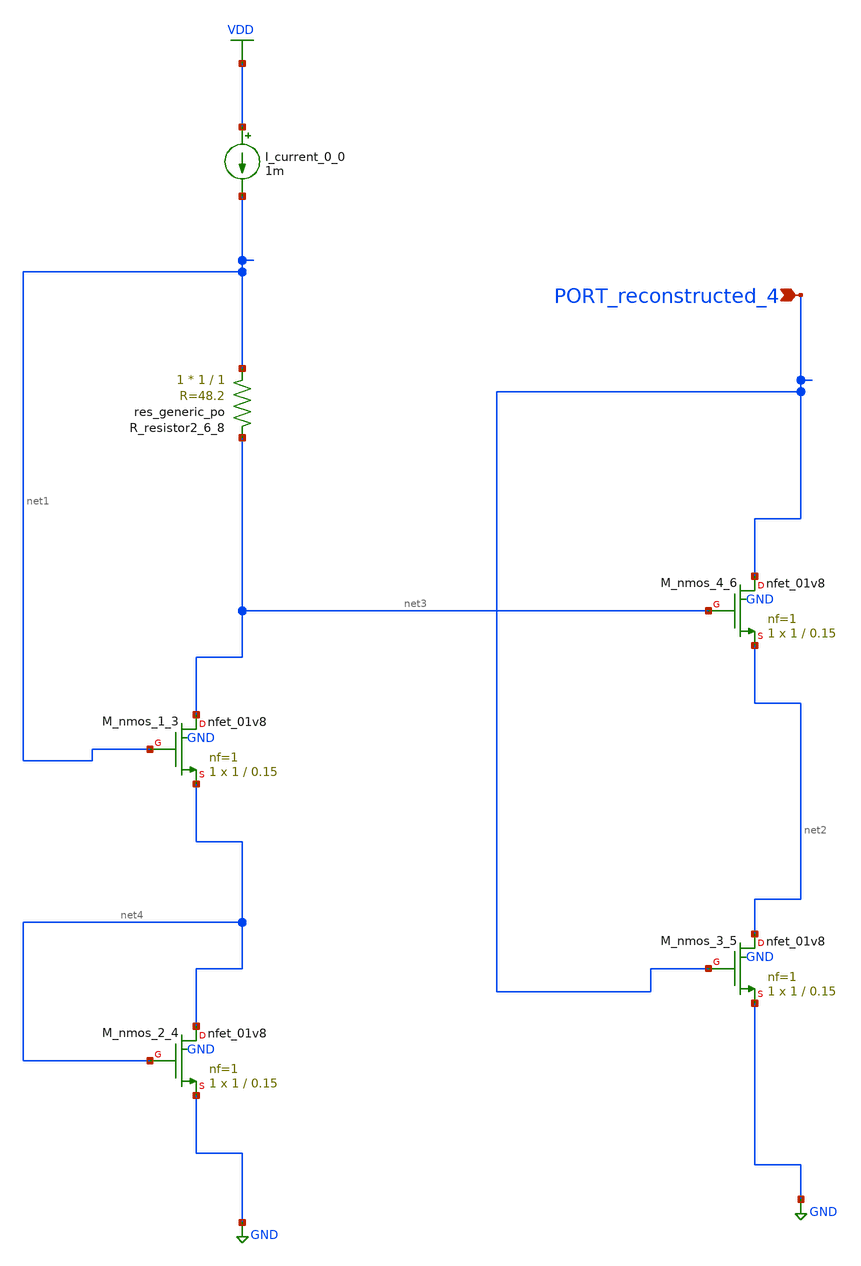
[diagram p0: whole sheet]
** sch_path: schematics/AMSNet/265.sch
**.subckt 265 PORT_reconstructed_4
*.ipin PORT_reconstructed_4
I_current_0_0 VDD net1 1m
XM_nmos_1_3 net3 net1 net4 GND sky130_fd_pr__nfet_01v8 L=0.15 W=1 nf=1 ad='int((1 + 1)/2) * 1 / 1 * 0.29'
+ as='int((1 + 2)/2) * 1 / 1 * 0.29' pd='2*int((1 + 1)/2) * (1 / 1 + 0.29)' ps='2*int((1 + 2)/2) * (1 / 1 + 0.29)'
+ nrd='0.29 / 1 ' nrs='0.29 / 1 ' sa=0 sb=0 sd=0 mult=1 m=1
XM_nmos_2_4 net4 net4 GND GND sky130_fd_pr__nfet_01v8 L=0.15 W=1 nf=1 ad='int((1 + 1)/2) * 1 / 1 * 0.29'
+ as='int((1 + 2)/2) * 1 / 1 * 0.29' pd='2*int((1 + 1)/2) * (1 / 1 + 0.29)' ps='2*int((1 + 2)/2) * (1 / 1 + 0.29)'
+ nrd='0.29 / 1 ' nrs='0.29 / 1 ' sa=0 sb=0 sd=0 mult=1 m=1
XM_nmos_3_5 net2 PORT_reconstructed_4 GND GND sky130_fd_pr__nfet_01v8 L=0.15 W=1 nf=1 ad='int((1 + 1)/2) * 1 / 1 * 0.29'
+ as='int((1 + 2)/2) * 1 / 1 * 0.29' pd='2*int((1 + 1)/2) * (1 / 1 + 0.29)' ps='2*int((1 + 2)/2) * (1 / 1 + 0.29)'
+ nrd='0.29 / 1 ' nrs='0.29 / 1 ' sa=0 sb=0 sd=0 mult=1 m=1
XM_nmos_4_6 PORT_reconstructed_4 net3 net2 GND sky130_fd_pr__nfet_01v8 L=0.15 W=1 nf=1 ad='int((1 + 1)/2) * 1 / 1 * 0.29'
+ as='int((1 + 2)/2) * 1 / 1 * 0.29' pd='2*int((1 + 1)/2) * (1 / 1 + 0.29)' ps='2*int((1 + 2)/2) * (1 / 1 + 0.29)'
+ nrd='0.29 / 1 ' nrs='0.29 / 1 ' sa=0 sb=0 sd=0 mult=1 m=1
XR_resistor2_6_8 net1 net3 sky130_fd_pr__res_generic_po W=1 L=1 m=1
**.ends
.GLOBAL GND
.GLOBAL VDD
.end
